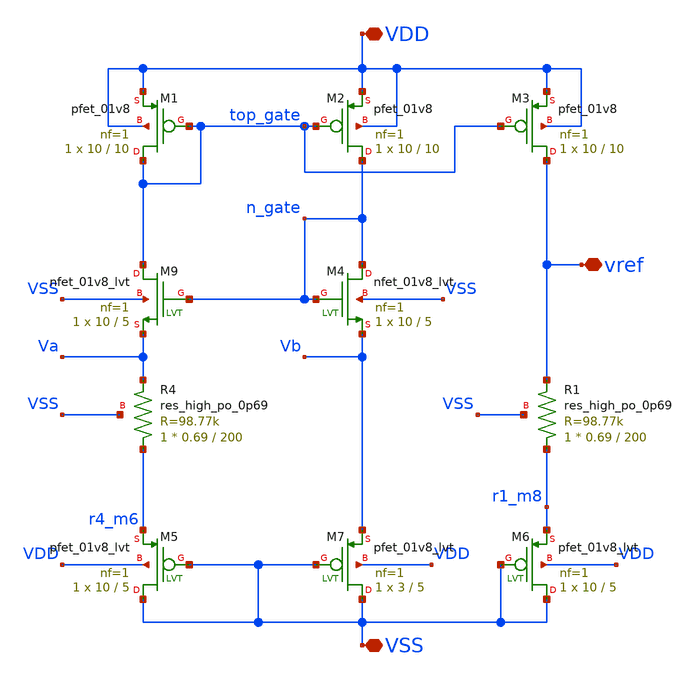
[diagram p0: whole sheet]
** sch_path: xschem/bandgap.sch
**.subckt bandgap VSS VDD vref
*.iopin VSS
*.iopin VDD
*.iopin vref
XM1 top_gate top_gate VDD VDD sky130_fd_pr__pfet_01v8 L=10 W=10 nf=1 ad='int((nf+1)/2) * W/nf * 0.29'
+ as='int((nf+2)/2) * W/nf * 0.29' pd='2*int((nf+1)/2) * (W/nf + 0.29)' ps='2*int((nf+2)/2) * (W/nf + 0.29)'
+ nrd='0.29 / W' nrs='0.29 / W' sa=0 sb=0 sd=0 mult=1 m=1
XM2 n_gate top_gate VDD VDD sky130_fd_pr__pfet_01v8 L=10 W=10 nf=1 ad='int((nf+1)/2) * W/nf * 0.29' as='int((nf+2)/2) * W/nf * 0.29'
+ pd='2*int((nf+1)/2) * (W/nf + 0.29)' ps='2*int((nf+2)/2) * (W/nf + 0.29)' nrd='0.29 / W' nrs='0.29 / W'
+ sa=0 sb=0 sd=0 mult=1 m=1
XM3 vref top_gate VDD VDD sky130_fd_pr__pfet_01v8 L=10 W=10 nf=1 ad='int((nf+1)/2) * W/nf * 0.29' as='int((nf+2)/2) * W/nf * 0.29'
+ pd='2*int((nf+1)/2) * (W/nf + 0.29)' ps='2*int((nf+2)/2) * (W/nf + 0.29)' nrd='0.29 / W' nrs='0.29 / W'
+ sa=0 sb=0 sd=0 mult=1 m=1
XR4 r4_m6 Va VSS sky130_fd_pr__res_high_po_0p69 L=200 mult=1 m=1
XR1 r1_m8 vref VSS sky130_fd_pr__res_high_po_0p69 L=200 mult=1 m=1
XM9 top_gate n_gate Va VSS sky130_fd_pr__nfet_01v8_lvt L=5 W=10 nf=1 ad='int((nf+1)/2) * W/nf * 0.29'
+ as='int((nf+2)/2) * W/nf * 0.29' pd='2*int((nf+1)/2) * (W/nf + 0.29)' ps='2*int((nf+2)/2) * (W/nf + 0.29)'
+ nrd='0.29 / W' nrs='0.29 / W' sa=0 sb=0 sd=0 mult=1 m=1
XM4 n_gate n_gate Vb VSS sky130_fd_pr__nfet_01v8_lvt L=5 W=10 nf=1 ad='int((nf+1)/2) * W/nf * 0.29' as='int((nf+2)/2) * W/nf * 0.29'
+ pd='2*int((nf+1)/2) * (W/nf + 0.29)' ps='2*int((nf+2)/2) * (W/nf + 0.29)' nrd='0.29 / W' nrs='0.29 / W'
+ sa=0 sb=0 sd=0 mult=1 m=1
XM5 VSS VSS r4_m6 VDD sky130_fd_pr__pfet_01v8_lvt L=5 W=10 nf=1 ad='int((nf+1)/2) * W/nf * 0.29' as='int((nf+2)/2) * W/nf * 0.29'
+ pd='2*int((nf+1)/2) * (W/nf + 0.29)' ps='2*int((nf+2)/2) * (W/nf + 0.29)' nrd='0.29 / W' nrs='0.29 / W'
+ sa=0 sb=0 sd=0 mult=1 m=1
XM6 VSS VSS r1_m8 VDD sky130_fd_pr__pfet_01v8_lvt L=5 W=10 nf=1 ad='int((nf+1)/2) * W/nf * 0.29' as='int((nf+2)/2) * W/nf * 0.29'
+ pd='2*int((nf+1)/2) * (W/nf + 0.29)' ps='2*int((nf+2)/2) * (W/nf + 0.29)' nrd='0.29 / W' nrs='0.29 / W'
+ sa=0 sb=0 sd=0 mult=1 m=1
XM7 VSS VSS Vb VDD sky130_fd_pr__pfet_01v8_lvt L=5 W=3 nf=1 ad='int((nf+1)/2) * W/nf * 0.29' as='int((nf+2)/2) * W/nf * 0.29'
+ pd='2*int((nf+1)/2) * (W/nf + 0.29)' ps='2*int((nf+2)/2) * (W/nf + 0.29)' nrd='0.29 / W' nrs='0.29 / W'
+ sa=0 sb=0 sd=0 mult=1 m=1
**.ends
.end
